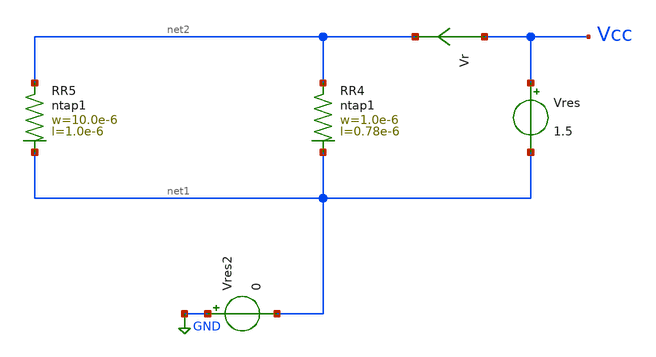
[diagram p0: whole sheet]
** sch_path: ihp-sg13g2/xschem_libs/sg13g2_tests_ase/dc_ntap1/schematic/dc_ntap1.sch
* Copyright 2023 IHP PDK Authors
**.subckt dc_ntap1
Vres Vcc net1 1.5
Vr Vcc net2 0
.save i(vr)
Vres2 GND net1 0
XR4 net2 net1 ntap1 R=225.8 w=1.0e-6 l=0.78e-6
XR5 net2 net1 ntap1 R=30.62 w=10.0e-6 l=1.0e-6
**.ends
.GLOBAL GND
.end
